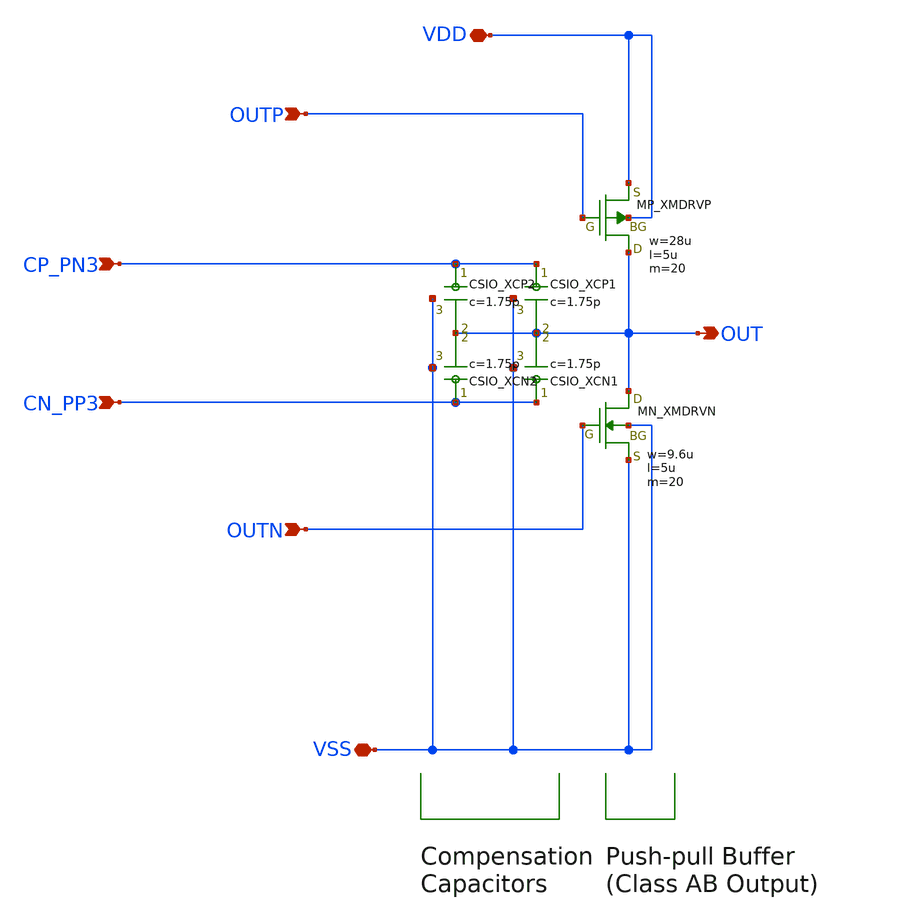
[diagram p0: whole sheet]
** sch_path: member_project/InstrumentationAmplifier/3zki/opamp_3zki_ina_first_2_half.sch
**.subckt opamp_3zki_ina_first_2_half VDD VSS OUT OUTP OUTN CP_PN3 CN_PP3
*.iopin VDD
*.iopin VSS
*.opin OUT
*.ipin OUTP
*.ipin OUTN
*.ipin CP_PN3
*.ipin CN_PP3
XMDRVP OUT OUTP VDD VDD PMOS w=28u l=5u as=21p ad=21p ps=17u pd=17u nrd=0 nrs=0 m=20
XMDRVN OUT OUTN VSS VSS NMOS w=9.6u l=5u as=7.2p ad=7.2p ps=7.8u pd=7.8u nrd=0 nrs=0 m=20
XCP1 CP_PN3 OUT VSS F_CSIO c=1.75p x=32.6u y=87.3u m=1
XCP2 CP_PN3 OUT VSS F_CSIO c=1.75p x=32.6u y=87.3u m=1
XCN1 CN_PP3 OUT VSS F_CSIO c=1.75p x=32.6u y=87.3u m=1
XCN2 CN_PP3 OUT VSS F_CSIO c=1.75p x=32.6u y=87.3u m=1
**.ends
.end
